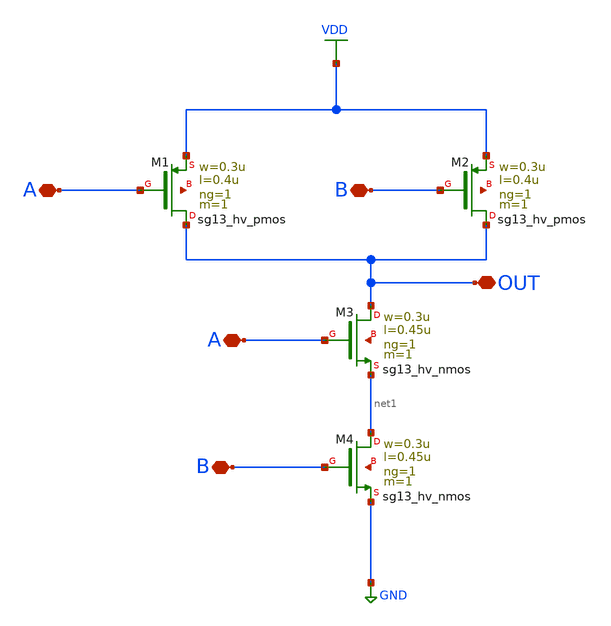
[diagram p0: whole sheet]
** sch_path: design/blocks/nandgate/schematic/nandgate.sch
**.subckt nandgate A A B B OUT
*.iopin A
*.iopin A
*.iopin B
*.iopin B
*.iopin OUT
XM1 OUT A VDD net2 sg13_hv_pmos w=0.3u l=0.4u ng=1 m=1 mm_ok=1
XM2 OUT B VDD net3 sg13_hv_pmos w=0.3u l=0.4u ng=1 m=1 mm_ok=1
XM3 OUT A net1 net4 sg13_hv_nmos w=0.3u l=0.45u ng=1 m=1 mm_ok=1
XM4 net1 B GND net5 sg13_hv_nmos w=0.3u l=0.45u ng=1 m=1 mm_ok=1
**.ends
.GLOBAL GND
.GLOBAL VDD
.end
